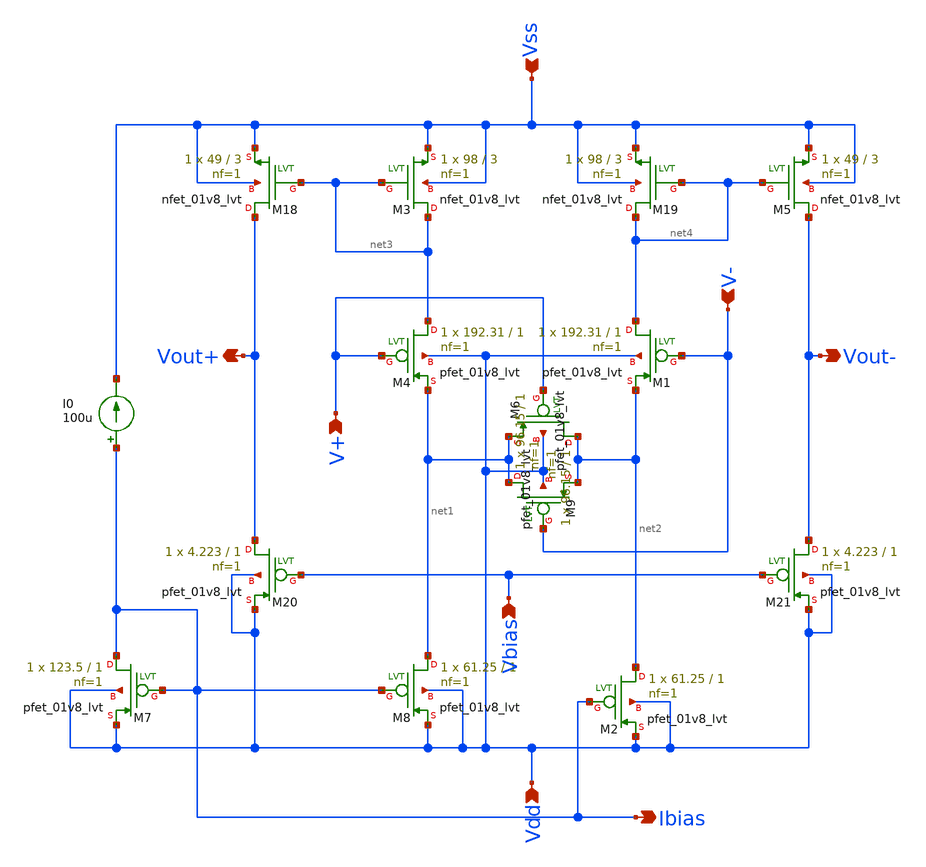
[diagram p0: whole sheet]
** sch_path: xschem/MY_OTA_Half.sch
**.subckt MY_OTA_Half Vout+ Vdd Vss V+ V- Vout- Vbias Ibias
*.opin Vout+
*.ipin Vdd
*.ipin Vss
*.ipin V+
*.ipin V-
*.opin Vout-
*.ipin Vbias
*.opin Ibias
XM7 Ibias Ibias Vdd Vdd sky130_fd_pr__pfet_01v8_lvt L=1 W=123.5 nf=1 ad='int((1 + 1)/2) * 123.5 / 1 * 0.29'
+ as='int((1 + 2)/2) * 123.5 / 1 * 0.29' pd='2*int((1 + 1)/2) * (123.5 / 1 + 0.29)' ps='2*int((1 + 2)/2) * (123.5 / 1 + 0.29)'
+ nrd='0.29 / 123.5 ' nrs='0.29 / 123.5 ' sa=0 sb=0 sd=0 mult=1 m=1
XM8 net1 Ibias Vdd Vdd sky130_fd_pr__pfet_01v8_lvt L=1 W=61.25 nf=1 ad='int((1 + 1)/2) * 61.25 / 1 * 0.29'
+ as='int((1 + 2)/2) * 61.25 / 1 * 0.29' pd='2*int((1 + 1)/2) * (61.25 / 1 + 0.29)' ps='2*int((1 + 2)/2) * (61.25 / 1 + 0.29)'
+ nrd='0.29 / 61.25 ' nrs='0.29 / 61.25 ' sa=0 sb=0 sd=0 mult=1 m=1
XM4 net3 V+ net1 Vdd sky130_fd_pr__pfet_01v8_lvt L=1 W=192.31 nf=1 ad='int((1 + 1)/2) * 192.31 / 1 * 0.29'
+ as='int((1 + 2)/2) * 192.31 / 1 * 0.29' pd='2*int((1 + 1)/2) * (192.31 / 1 + 0.29)' ps='2*int((1 + 2)/2) * (192.31 / 1 + 0.29)'
+ nrd='0.29 / 192.31 ' nrs='0.29 / 192.31 ' sa=0 sb=0 sd=0 mult=1 m=1
XM1 net4 V- net2 Vdd sky130_fd_pr__pfet_01v8_lvt L=1 W=192.31 nf=1 ad='int((1 + 1)/2) * 192.31 / 1 * 0.29'
+ as='int((1 + 2)/2) * 192.31 / 1 * 0.29' pd='2*int((1 + 1)/2) * (192.31 / 1 + 0.29)' ps='2*int((1 + 2)/2) * (192.31 / 1 + 0.29)'
+ nrd='0.29 / 192.31 ' nrs='0.29 / 192.31 ' sa=0 sb=0 sd=0 mult=1 m=1
XM3 net3 net3 Vss Vss sky130_fd_pr__nfet_01v8_lvt L=3 W=98 nf=1 ad='int((1 + 1)/2) * 98 / 1 * 0.29' as='int((1 + 2)/2) * 98 / 1 * 0.29'
+ pd='2*int((1 + 1)/2) * (98 / 1 + 0.29)' ps='2*int((1 + 2)/2) * (98 / 1 + 0.29)' nrd='0.29 / 98 ' nrs='0.29 / 98 '
+ sa=0 sb=0 sd=0 mult=1 m=1
XM2 net2 Ibias Vdd Vdd sky130_fd_pr__pfet_01v8_lvt L=1 W=61.25 nf=1 ad='int((1 + 1)/2) * 61.25 / 1 * 0.29'
+ as='int((1 + 2)/2) * 61.25 / 1 * 0.29' pd='2*int((1 + 1)/2) * (61.25 / 1 + 0.29)' ps='2*int((1 + 2)/2) * (61.25 / 1 + 0.29)'
+ nrd='0.29 / 61.25 ' nrs='0.29 / 61.25 ' sa=0 sb=0 sd=0 mult=1 m=1
XM6 net2 V+ net1 Vdd sky130_fd_pr__pfet_01v8_lvt L=1 W=96.15 nf=1 ad='int((1 + 1)/2) * 96.15 / 1 * 0.29'
+ as='int((1 + 2)/2) * 96.15 / 1 * 0.29' pd='2*int((1 + 1)/2) * (96.15 / 1 + 0.29)' ps='2*int((1 + 2)/2) * (96.15 / 1 + 0.29)'
+ nrd='0.29 / 96.15 ' nrs='0.29 / 96.15 ' sa=0 sb=0 sd=0 mult=1 m=1
XM9 net1 V- net2 Vdd sky130_fd_pr__pfet_01v8_lvt L=1 W=96.15 nf=1 ad='int((1 + 1)/2) * 96.15 / 1 * 0.29'
+ as='int((1 + 2)/2) * 96.15 / 1 * 0.29' pd='2*int((1 + 1)/2) * (96.15 / 1 + 0.29)' ps='2*int((1 + 2)/2) * (96.15 / 1 + 0.29)'
+ nrd='0.29 / 96.15 ' nrs='0.29 / 96.15 ' sa=0 sb=0 sd=0 mult=1 m=1
XM18 Vout+ net3 Vss Vss sky130_fd_pr__nfet_01v8_lvt L=3 W=49 nf=1 ad='int((1 + 1)/2) * 49 / 1 * 0.29'
+ as='int((1 + 2)/2) * 49 / 1 * 0.29' pd='2*int((1 + 1)/2) * (49 / 1 + 0.29)' ps='2*int((1 + 2)/2) * (49 / 1 + 0.29)'
+ nrd='0.29 / 49 ' nrs='0.29 / 49 ' sa=0 sb=0 sd=0 mult=1 m=1
XM5 Vout- net4 Vss Vss sky130_fd_pr__nfet_01v8_lvt L=3 W=49 nf=1 ad='int((1 + 1)/2) * 49 / 1 * 0.29'
+ as='int((1 + 2)/2) * 49 / 1 * 0.29' pd='2*int((1 + 1)/2) * (49 / 1 + 0.29)' ps='2*int((1 + 2)/2) * (49 / 1 + 0.29)'
+ nrd='0.29 / 49 ' nrs='0.29 / 49 ' sa=0 sb=0 sd=0 mult=1 m=1
XM19 net4 net4 Vss Vss sky130_fd_pr__nfet_01v8_lvt L=3 W=98 nf=1 ad='int((1 + 1)/2) * 98 / 1 * 0.29'
+ as='int((1 + 2)/2) * 98 / 1 * 0.29' pd='2*int((1 + 1)/2) * (98 / 1 + 0.29)' ps='2*int((1 + 2)/2) * (98 / 1 + 0.29)'
+ nrd='0.29 / 98 ' nrs='0.29 / 98 ' sa=0 sb=0 sd=0 mult=1 m=1
XM20 Vout+ Vbias Vdd Vdd sky130_fd_pr__pfet_01v8_lvt L=1 W=4.223 nf=1 ad='int((1 + 1)/2) * 4.223 / 1 * 0.29'
+ as='int((1 + 2)/2) * 4.223 / 1 * 0.29' pd='2*int((1 + 1)/2) * (4.223 / 1 + 0.29)' ps='2*int((1 + 2)/2) * (4.223 / 1 + 0.29)'
+ nrd='0.29 / 4.223 ' nrs='0.29 / 4.223 ' sa=0 sb=0 sd=0 mult=1 m=1
XM21 Vout- Vbias Vdd Vdd sky130_fd_pr__pfet_01v8_lvt L=1 W=4.223 nf=1 ad='int((1 + 1)/2) * 4.223 / 1 * 0.29'
+ as='int((1 + 2)/2) * 4.223 / 1 * 0.29' pd='2*int((1 + 1)/2) * (4.223 / 1 + 0.29)' ps='2*int((1 + 2)/2) * (4.223 / 1 + 0.29)'
+ nrd='0.29 / 4.223 ' nrs='0.29 / 4.223 ' sa=0 sb=0 sd=0 mult=1 m=1
I0 Ibias Vss 100u
**.ends
.end
